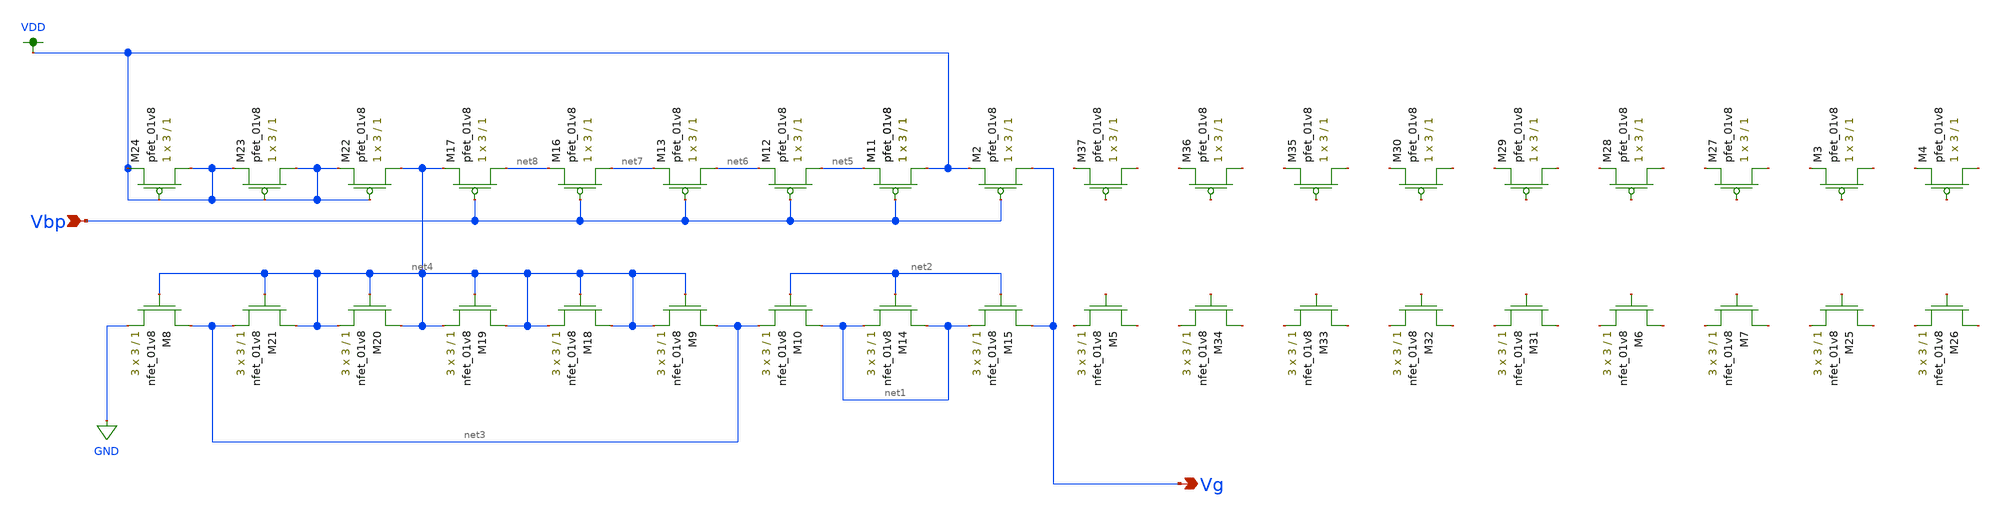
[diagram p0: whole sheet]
** sch_path: schematic/LDS/bias_cascode.sch
**.subckt bias_cascode Vbp Vg
*.ipin Vbp
*.opin Vg
XM1 VDD Vbp net5 VDD sky130_fd_pr__pfet_01v8 L=1 W=3 nf=1 ad='int((nf+1)/2) * W/nf * 0.29' as='int((nf+2)/2) * W/nf * 0.29'
+ pd='2*int((nf+1)/2) * (W/nf + 0.29)' ps='2*int((nf+2)/2) * (W/nf + 0.29)' nrd='0.29 / W' nrs='0.29 / W'
+ sa=0 sb=0 sd=0 mult=1 m=1
XM2 Vg Vbp VDD VDD sky130_fd_pr__pfet_01v8 L=1 W=3 nf=1 ad='int((nf+1)/2) * W/nf * 0.29' as='int((nf+2)/2) * W/nf * 0.29'
+ pd='2*int((nf+1)/2) * (W/nf + 0.29)' ps='2*int((nf+2)/2) * (W/nf + 0.29)' nrd='0.29 / W' nrs='0.29 / W'
+ sa=0 sb=0 sd=0 mult=1 m=1
XM8 net3 net4 GND GND sky130_fd_pr__nfet_01v8 L=1 W=3 nf=1 ad='int((nf+1)/2) * W/nf * 0.29' as='int((nf+2)/2) * W/nf * 0.29'
+ pd='2*int((nf+1)/2) * (W/nf + 0.29)' ps='2*int((nf+2)/2) * (W/nf + 0.29)' nrd='0.29 / W' nrs='0.29 / W'
+ sa=0 sb=0 sd=0 mult=3 m=3
XM9 net3 net4 net4 GND sky130_fd_pr__nfet_01v8 L=1 W=3 nf=1 ad='int((nf+1)/2) * W/nf * 0.29' as='int((nf+2)/2) * W/nf * 0.29'
+ pd='2*int((nf+1)/2) * (W/nf + 0.29)' ps='2*int((nf+2)/2) * (W/nf + 0.29)' nrd='0.29 / W' nrs='0.29 / W'
+ sa=0 sb=0 sd=0 mult=3 m=3
XM10 net1 net2 net3 GND sky130_fd_pr__nfet_01v8 L=1 W=3 nf=1 ad='int((nf+1)/2) * W/nf * 0.29' as='int((nf+2)/2) * W/nf * 0.29'
+ pd='2*int((nf+1)/2) * (W/nf + 0.29)' ps='2*int((nf+2)/2) * (W/nf + 0.29)' nrd='0.29 / W' nrs='0.29 / W'
+ sa=0 sb=0 sd=0 mult=3 m=3
XM11 VDD Vbp net5 VDD sky130_fd_pr__pfet_01v8 L=1 W=3 nf=1 ad='int((nf+1)/2) * W/nf * 0.29' as='int((nf+2)/2) * W/nf * 0.29'
+ pd='2*int((nf+1)/2) * (W/nf + 0.29)' ps='2*int((nf+2)/2) * (W/nf + 0.29)' nrd='0.29 / W' nrs='0.29 / W'
+ sa=0 sb=0 sd=0 mult=1 m=1
XM14 net1 net2 net1 GND sky130_fd_pr__nfet_01v8 L=1 W=3 nf=1 ad='int((nf+1)/2) * W/nf * 0.29' as='int((nf+2)/2) * W/nf * 0.29'
+ pd='2*int((nf+1)/2) * (W/nf + 0.29)' ps='2*int((nf+2)/2) * (W/nf + 0.29)' nrd='0.29 / W' nrs='0.29 / W'
+ sa=0 sb=0 sd=0 mult=3 m=3
XM15 Vg net2 net1 GND sky130_fd_pr__nfet_01v8 L=1 W=3 nf=1 ad='int((nf+1)/2) * W/nf * 0.29' as='int((nf+2)/2) * W/nf * 0.29'
+ pd='2*int((nf+1)/2) * (W/nf + 0.29)' ps='2*int((nf+2)/2) * (W/nf + 0.29)' nrd='0.29 / W' nrs='0.29 / W'
+ sa=0 sb=0 sd=0 mult=3 m=3
XM12 net5 Vbp net6 VDD sky130_fd_pr__pfet_01v8 L=1 W=3 nf=1 ad='int((nf+1)/2) * W/nf * 0.29' as='int((nf+2)/2) * W/nf * 0.29'
+ pd='2*int((nf+1)/2) * (W/nf + 0.29)' ps='2*int((nf+2)/2) * (W/nf + 0.29)' nrd='0.29 / W' nrs='0.29 / W'
+ sa=0 sb=0 sd=0 mult=1 m=1
XM13 net6 Vbp net7 VDD sky130_fd_pr__pfet_01v8 L=1 W=3 nf=1 ad='int((nf+1)/2) * W/nf * 0.29' as='int((nf+2)/2) * W/nf * 0.29'
+ pd='2*int((nf+1)/2) * (W/nf + 0.29)' ps='2*int((nf+2)/2) * (W/nf + 0.29)' nrd='0.29 / W' nrs='0.29 / W'
+ sa=0 sb=0 sd=0 mult=1 m=1
XM16 net7 Vbp net8 VDD sky130_fd_pr__pfet_01v8 L=1 W=3 nf=1 ad='int((nf+1)/2) * W/nf * 0.29' as='int((nf+2)/2) * W/nf * 0.29'
+ pd='2*int((nf+1)/2) * (W/nf + 0.29)' ps='2*int((nf+2)/2) * (W/nf + 0.29)' nrd='0.29 / W' nrs='0.29 / W'
+ sa=0 sb=0 sd=0 mult=1 m=1
XM17 net8 Vbp net4 VDD sky130_fd_pr__pfet_01v8 L=1 W=3 nf=1 ad='int((nf+1)/2) * W/nf * 0.29' as='int((nf+2)/2) * W/nf * 0.29'
+ pd='2*int((nf+1)/2) * (W/nf + 0.29)' ps='2*int((nf+2)/2) * (W/nf + 0.29)' nrd='0.29 / W' nrs='0.29 / W'
+ sa=0 sb=0 sd=0 mult=1 m=1
XM18 net4 net4 net4 GND sky130_fd_pr__nfet_01v8 L=1 W=3 nf=1 ad='int((nf+1)/2) * W/nf * 0.29' as='int((nf+2)/2) * W/nf * 0.29'
+ pd='2*int((nf+1)/2) * (W/nf + 0.29)' ps='2*int((nf+2)/2) * (W/nf + 0.29)' nrd='0.29 / W' nrs='0.29 / W'
+ sa=0 sb=0 sd=0 mult=3 m=3
XM19 net4 net4 net4 GND sky130_fd_pr__nfet_01v8 L=1 W=3 nf=1 ad='int((nf+1)/2) * W/nf * 0.29' as='int((nf+2)/2) * W/nf * 0.29'
+ pd='2*int((nf+1)/2) * (W/nf + 0.29)' ps='2*int((nf+2)/2) * (W/nf + 0.29)' nrd='0.29 / W' nrs='0.29 / W'
+ sa=0 sb=0 sd=0 mult=3 m=3
XM20 net4 net4 net4 GND sky130_fd_pr__nfet_01v8 L=1 W=3 nf=1 ad='int((nf+1)/2) * W/nf * 0.29' as='int((nf+2)/2) * W/nf * 0.29'
+ pd='2*int((nf+1)/2) * (W/nf + 0.29)' ps='2*int((nf+2)/2) * (W/nf + 0.29)' nrd='0.29 / W' nrs='0.29 / W'
+ sa=0 sb=0 sd=0 mult=3 m=3
XM21 net4 net4 net3 GND sky130_fd_pr__nfet_01v8 L=1 W=3 nf=1 ad='int((nf+1)/2) * W/nf * 0.29' as='int((nf+2)/2) * W/nf * 0.29'
+ pd='2*int((nf+1)/2) * (W/nf + 0.29)' ps='2*int((nf+2)/2) * (W/nf + 0.29)' nrd='0.29 / W' nrs='0.29 / W'
+ sa=0 sb=0 sd=0 mult=3 m=3
XM22 net4 VDD VDD VDD sky130_fd_pr__pfet_01v8 L=1 W=3 nf=1 ad='int((nf+1)/2) * W/nf * 0.29' as='int((nf+2)/2) * W/nf * 0.29'
+ pd='2*int((nf+1)/2) * (W/nf + 0.29)' ps='2*int((nf+2)/2) * (W/nf + 0.29)' nrd='0.29 / W' nrs='0.29 / W'
+ sa=0 sb=0 sd=0 mult=1 m=1
XM23 VDD VDD VDD VDD sky130_fd_pr__pfet_01v8 L=1 W=3 nf=1 ad='int((nf+1)/2) * W/nf * 0.29' as='int((nf+2)/2) * W/nf * 0.29'
+ pd='2*int((nf+1)/2) * (W/nf + 0.29)' ps='2*int((nf+2)/2) * (W/nf + 0.29)' nrd='0.29 / W' nrs='0.29 / W'
+ sa=0 sb=0 sd=0 mult=1 m=1
XM24 VDD VDD VDD VDD sky130_fd_pr__pfet_01v8 L=1 W=3 nf=1 ad='int((nf+1)/2) * W/nf * 0.29' as='int((nf+2)/2) * W/nf * 0.29'
+ pd='2*int((nf+1)/2) * (W/nf + 0.29)' ps='2*int((nf+2)/2) * (W/nf + 0.29)' nrd='0.29 / W' nrs='0.29 / W'
+ sa=0 sb=0 sd=0 mult=1 m=1
XM3 net9 net10 net11 VDD sky130_fd_pr__pfet_01v8 L=1 W=3 nf=1 ad='int((nf+1)/2) * W/nf * 0.29' as='int((nf+2)/2) * W/nf * 0.29'
+ pd='2*int((nf+1)/2) * (W/nf + 0.29)' ps='2*int((nf+2)/2) * (W/nf + 0.29)' nrd='0.29 / W' nrs='0.29 / W'
+ sa=0 sb=0 sd=0 mult=1 m=1
XM4 net12 net13 net14 VDD sky130_fd_pr__pfet_01v8 L=1 W=3 nf=1 ad='int((nf+1)/2) * W/nf * 0.29' as='int((nf+2)/2) * W/nf * 0.29'
+ pd='2*int((nf+1)/2) * (W/nf + 0.29)' ps='2*int((nf+2)/2) * (W/nf + 0.29)' nrd='0.29 / W' nrs='0.29 / W'
+ sa=0 sb=0 sd=0 mult=1 m=1
XM5 net15 net16 net17 GND sky130_fd_pr__nfet_01v8 L=1 W=3 nf=1 ad='int((nf+1)/2) * W/nf * 0.29' as='int((nf+2)/2) * W/nf * 0.29'
+ pd='2*int((nf+1)/2) * (W/nf + 0.29)' ps='2*int((nf+2)/2) * (W/nf + 0.29)' nrd='0.29 / W' nrs='0.29 / W'
+ sa=0 sb=0 sd=0 mult=3 m=3
XM6 net18 net19 net20 GND sky130_fd_pr__nfet_01v8 L=1 W=3 nf=1 ad='int((nf+1)/2) * W/nf * 0.29' as='int((nf+2)/2) * W/nf * 0.29'
+ pd='2*int((nf+1)/2) * (W/nf + 0.29)' ps='2*int((nf+2)/2) * (W/nf + 0.29)' nrd='0.29 / W' nrs='0.29 / W'
+ sa=0 sb=0 sd=0 mult=3 m=3
XM7 net21 net22 net23 GND sky130_fd_pr__nfet_01v8 L=1 W=3 nf=1 ad='int((nf+1)/2) * W/nf * 0.29' as='int((nf+2)/2) * W/nf * 0.29'
+ pd='2*int((nf+1)/2) * (W/nf + 0.29)' ps='2*int((nf+2)/2) * (W/nf + 0.29)' nrd='0.29 / W' nrs='0.29 / W'
+ sa=0 sb=0 sd=0 mult=3 m=3
XM25 net24 net25 net26 GND sky130_fd_pr__nfet_01v8 L=1 W=3 nf=1 ad='int((nf+1)/2) * W/nf * 0.29' as='int((nf+2)/2) * W/nf * 0.29'
+ pd='2*int((nf+1)/2) * (W/nf + 0.29)' ps='2*int((nf+2)/2) * (W/nf + 0.29)' nrd='0.29 / W' nrs='0.29 / W'
+ sa=0 sb=0 sd=0 mult=3 m=3
XM26 net27 net28 net29 GND sky130_fd_pr__nfet_01v8 L=1 W=3 nf=1 ad='int((nf+1)/2) * W/nf * 0.29' as='int((nf+2)/2) * W/nf * 0.29'
+ pd='2*int((nf+1)/2) * (W/nf + 0.29)' ps='2*int((nf+2)/2) * (W/nf + 0.29)' nrd='0.29 / W' nrs='0.29 / W'
+ sa=0 sb=0 sd=0 mult=3 m=3
XM27 net30 net31 net32 VDD sky130_fd_pr__pfet_01v8 L=1 W=3 nf=1 ad='int((nf+1)/2) * W/nf * 0.29' as='int((nf+2)/2) * W/nf * 0.29'
+ pd='2*int((nf+1)/2) * (W/nf + 0.29)' ps='2*int((nf+2)/2) * (W/nf + 0.29)' nrd='0.29 / W' nrs='0.29 / W'
+ sa=0 sb=0 sd=0 mult=1 m=1
XM28 net33 net34 net35 VDD sky130_fd_pr__pfet_01v8 L=1 W=3 nf=1 ad='int((nf+1)/2) * W/nf * 0.29' as='int((nf+2)/2) * W/nf * 0.29'
+ pd='2*int((nf+1)/2) * (W/nf + 0.29)' ps='2*int((nf+2)/2) * (W/nf + 0.29)' nrd='0.29 / W' nrs='0.29 / W'
+ sa=0 sb=0 sd=0 mult=1 m=1
XM29 net36 net37 net38 VDD sky130_fd_pr__pfet_01v8 L=1 W=3 nf=1 ad='int((nf+1)/2) * W/nf * 0.29' as='int((nf+2)/2) * W/nf * 0.29'
+ pd='2*int((nf+1)/2) * (W/nf + 0.29)' ps='2*int((nf+2)/2) * (W/nf + 0.29)' nrd='0.29 / W' nrs='0.29 / W'
+ sa=0 sb=0 sd=0 mult=1 m=1
XM30 net39 net40 net41 VDD sky130_fd_pr__pfet_01v8 L=1 W=3 nf=1 ad='int((nf+1)/2) * W/nf * 0.29' as='int((nf+2)/2) * W/nf * 0.29'
+ pd='2*int((nf+1)/2) * (W/nf + 0.29)' ps='2*int((nf+2)/2) * (W/nf + 0.29)' nrd='0.29 / W' nrs='0.29 / W'
+ sa=0 sb=0 sd=0 mult=1 m=1
XM31 net42 net43 net44 GND sky130_fd_pr__nfet_01v8 L=1 W=3 nf=1 ad='int((nf+1)/2) * W/nf * 0.29' as='int((nf+2)/2) * W/nf * 0.29'
+ pd='2*int((nf+1)/2) * (W/nf + 0.29)' ps='2*int((nf+2)/2) * (W/nf + 0.29)' nrd='0.29 / W' nrs='0.29 / W'
+ sa=0 sb=0 sd=0 mult=3 m=3
XM32 net45 net46 net47 GND sky130_fd_pr__nfet_01v8 L=1 W=3 nf=1 ad='int((nf+1)/2) * W/nf * 0.29' as='int((nf+2)/2) * W/nf * 0.29'
+ pd='2*int((nf+1)/2) * (W/nf + 0.29)' ps='2*int((nf+2)/2) * (W/nf + 0.29)' nrd='0.29 / W' nrs='0.29 / W'
+ sa=0 sb=0 sd=0 mult=3 m=3
XM33 net48 net49 net50 GND sky130_fd_pr__nfet_01v8 L=1 W=3 nf=1 ad='int((nf+1)/2) * W/nf * 0.29' as='int((nf+2)/2) * W/nf * 0.29'
+ pd='2*int((nf+1)/2) * (W/nf + 0.29)' ps='2*int((nf+2)/2) * (W/nf + 0.29)' nrd='0.29 / W' nrs='0.29 / W'
+ sa=0 sb=0 sd=0 mult=3 m=3
XM34 net51 net52 net53 GND sky130_fd_pr__nfet_01v8 L=1 W=3 nf=1 ad='int((nf+1)/2) * W/nf * 0.29' as='int((nf+2)/2) * W/nf * 0.29'
+ pd='2*int((nf+1)/2) * (W/nf + 0.29)' ps='2*int((nf+2)/2) * (W/nf + 0.29)' nrd='0.29 / W' nrs='0.29 / W'
+ sa=0 sb=0 sd=0 mult=3 m=3
XM35 net54 net55 net56 VDD sky130_fd_pr__pfet_01v8 L=1 W=3 nf=1 ad='int((nf+1)/2) * W/nf * 0.29' as='int((nf+2)/2) * W/nf * 0.29'
+ pd='2*int((nf+1)/2) * (W/nf + 0.29)' ps='2*int((nf+2)/2) * (W/nf + 0.29)' nrd='0.29 / W' nrs='0.29 / W'
+ sa=0 sb=0 sd=0 mult=1 m=1
XM36 net57 net58 net59 VDD sky130_fd_pr__pfet_01v8 L=1 W=3 nf=1 ad='int((nf+1)/2) * W/nf * 0.29' as='int((nf+2)/2) * W/nf * 0.29'
+ pd='2*int((nf+1)/2) * (W/nf + 0.29)' ps='2*int((nf+2)/2) * (W/nf + 0.29)' nrd='0.29 / W' nrs='0.29 / W'
+ sa=0 sb=0 sd=0 mult=1 m=1
XM37 net60 net61 net62 VDD sky130_fd_pr__pfet_01v8 L=1 W=3 nf=1 ad='int((nf+1)/2) * W/nf * 0.29' as='int((nf+2)/2) * W/nf * 0.29'
+ pd='2*int((nf+1)/2) * (W/nf + 0.29)' ps='2*int((nf+2)/2) * (W/nf + 0.29)' nrd='0.29 / W' nrs='0.29 / W'
+ sa=0 sb=0 sd=0 mult=1 m=1
**.ends
.GLOBAL VDD
.GLOBAL GND
.end
